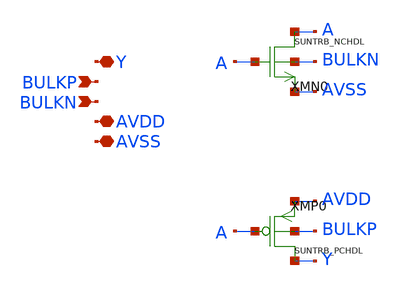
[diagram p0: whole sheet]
** sch_path: design/SUN_TRB_SKY130NM/SUNTRB_TIEH_CV.sch
**.subckt SUNTRB_TIEH_CV Y BULKP BULKN AVDD AVSS
*.iopin Y
*.ipin BULKP
*.ipin BULKN
*.iopin AVDD
*.iopin AVSS
XMN0 A A AVSS BULKN SUNTRB_NCHDL xoffset=0 yoffset=0 angle=0
XMP0 Y A AVDD BULKP SUNTRB_PCHDL xoffset=0 yoffset=0 angle=0 M=1
**.ends
.end
